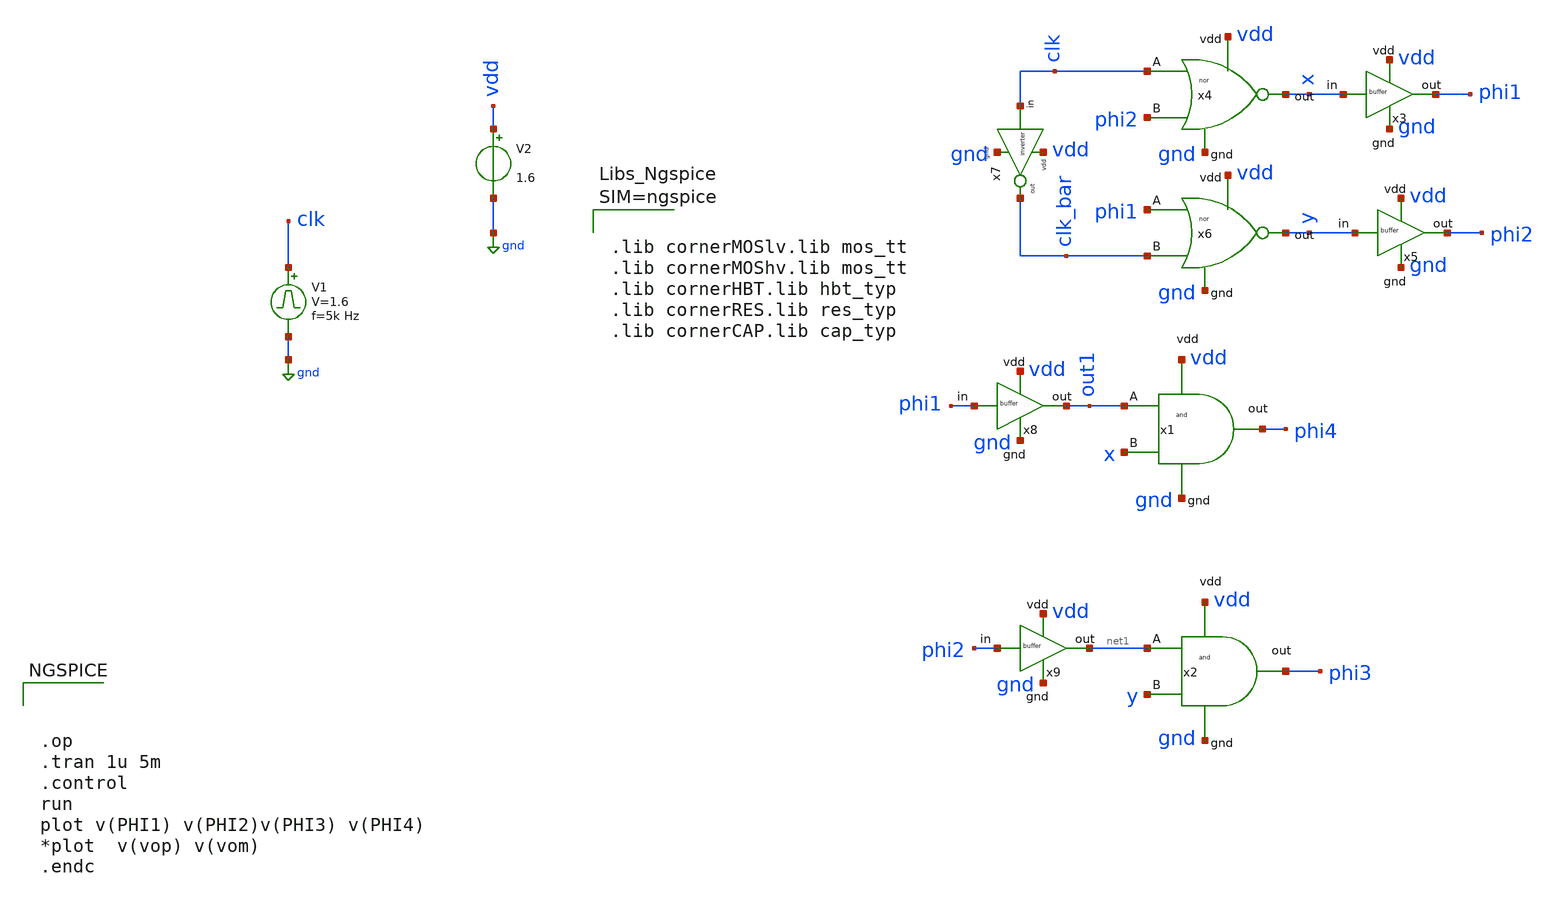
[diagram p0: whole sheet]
** sch_path: dependencies/OTA/OTA-main/schematic/xschem/top_module.sch
**.subckt top_module
x1 vdd x out1 gnd phi4 and
x2 vdd y net1 gnd phi3 and
x4 vdd phi2 clk gnd x nor
x6 vdd clk_bar phi1 gnd y nor
x7 clk clk_bar vdd gnd inverter
x8 phi1 out1 vdd gnd buffer
x9 phi2 net1 vdd gnd buffer
V2 vdd gnd 1.6
V1 clk gnd pulse 0 1.6 '0.495/ 5k ' '0.01/5k ' '0.01/5k ' '0.49/5k ' '1/5k '
x3 x phi1 vdd gnd buffer
x5 y phi2 vdd gnd buffer
**** begin user architecture code



.lib cornerMOSlv.lib mos_tt
.lib cornerMOShv.lib mos_tt
.lib cornerHBT.lib hbt_typ
.lib cornerRES.lib res_typ
.lib cornerCAP.lib cap_typ






.op
.tran 1u 5m
.control
run
plot v(PHI1) v(PHI2)v(PHI3) v(PHI4)
*plot  v(vop) v(vom)
.endc


**** end user architecture code
**.ends
.GLOBAL gnd
.end
